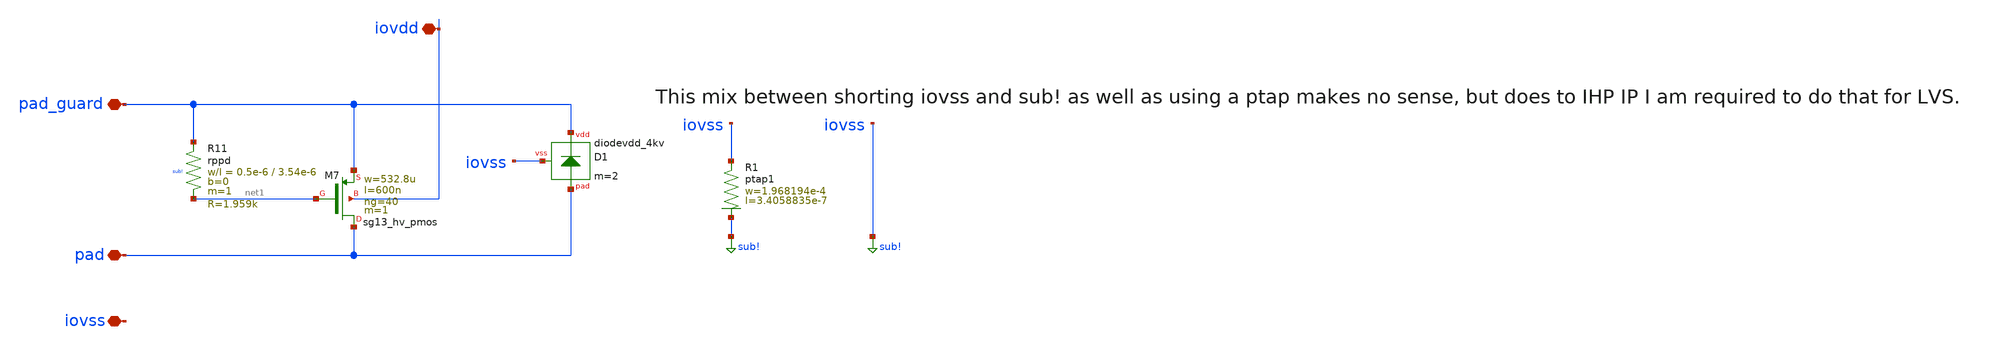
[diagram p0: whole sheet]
** sch_path: trident_test_structures/design_data/xschem/IOPadAnalogGuardLayer/pad_guard_to_vdd_first_stage_esd.sch
**.subckt pad_guard_to_vdd_first_stage_esd iovss pad pad_guard iovdd
*.iopin iovss
*.iopin pad
*.iopin pad_guard
*.iopin iovdd
XM7 pad net1 pad_guard iovdd sg13_hv_pmos w=532.8u l=600n ng=40 m=1 mm_ok=1
XR11 pad_guard net1 sub! rppd w=0.5e-6 l=3.54e-6 m=1 b=0 mm_ok=1
XD1 pad_guard pad iovss diodevdd_4kv m=2
XR1 iovss sub! ptap1 R=2.124 w=1.968194e-4 l=3.4058835e-7
**.ends
.GLOBAL sub!
.end
